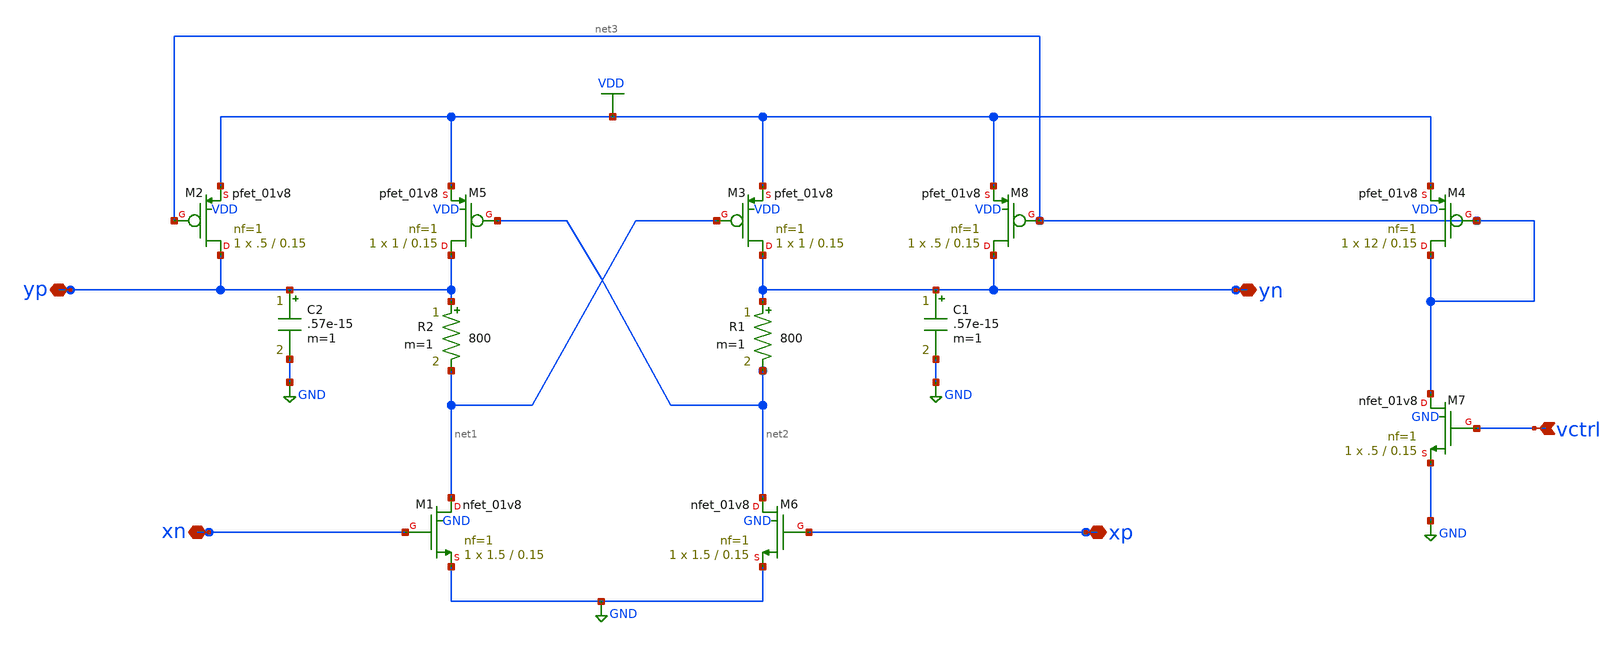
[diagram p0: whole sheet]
** sch_path: delay_cell/Delay_cell_2.sch
**.subckt Delay_cell_2 yp xn xp yn vctrl
*.iopin yp
*.iopin xn
*.iopin xp
*.iopin yn
*.ipin vctrl
R2 yp net1 800 m=1
R1 yn net2 800 m=1
XM4 net3 net3 VDD VDD sky130_fd_pr__pfet_01v8 L=0.15 W=12 nf=1 ad='int((nf+1)/2) * W/nf * 0.29' as='int((nf+2)/2) * W/nf * 0.29'
+ pd='2*int((nf+1)/2) * (W/nf + 0.29)' ps='2*int((nf+2)/2) * (W/nf + 0.29)' nrd='0.29 / W' nrs='0.29 / W'
+ sa=0 sb=0 sd=0 mult=1 m=1
XM7 net3 vctrl GND GND sky130_fd_pr__nfet_01v8 L=0.15 W=.5 nf=1 ad='int((nf+1)/2) * W/nf * 0.29' as='int((nf+2)/2) * W/nf * 0.29'
+ pd='2*int((nf+1)/2) * (W/nf + 0.29)' ps='2*int((nf+2)/2) * (W/nf + 0.29)' nrd='0.29 / W' nrs='0.29 / W'
+ sa=0 sb=0 sd=0 mult=1 m=1
C1 yn GND .57e-15 m=1
C2 yp GND .57e-15 m=1
XM1 net1 xn GND GND sky130_fd_pr__nfet_01v8 L=0.15 W=1.5 nf=1 ad='int((nf+1)/2) * W/nf * 0.29' as='int((nf+2)/2) * W/nf * 0.29'
+ pd='2*int((nf+1)/2) * (W/nf + 0.29)' ps='2*int((nf+2)/2) * (W/nf + 0.29)' nrd='0.29 / W' nrs='0.29 / W'
+ sa=0 sb=0 sd=0 mult=1 m=1
XM6 net2 xp GND GND sky130_fd_pr__nfet_01v8 L=0.15 W=1.5 nf=1 ad='int((nf+1)/2) * W/nf * 0.29' as='int((nf+2)/2) * W/nf * 0.29'
+ pd='2*int((nf+1)/2) * (W/nf + 0.29)' ps='2*int((nf+2)/2) * (W/nf + 0.29)' nrd='0.29 / W' nrs='0.29 / W'
+ sa=0 sb=0 sd=0 mult=1 m=1
XM2 yp net3 VDD VDD sky130_fd_pr__pfet_01v8 L=0.15 W=.5 nf=1 ad='int((nf+1)/2) * W/nf * 0.29' as='int((nf+2)/2) * W/nf * 0.29'
+ pd='2*int((nf+1)/2) * (W/nf + 0.29)' ps='2*int((nf+2)/2) * (W/nf + 0.29)' nrd='0.29 / W' nrs='0.29 / W'
+ sa=0 sb=0 sd=0 mult=1 m=1
XM3 yn net1 VDD VDD sky130_fd_pr__pfet_01v8 L=0.15 W=1 nf=1 ad='int((nf+1)/2) * W/nf * 0.29' as='int((nf+2)/2) * W/nf * 0.29'
+ pd='2*int((nf+1)/2) * (W/nf + 0.29)' ps='2*int((nf+2)/2) * (W/nf + 0.29)' nrd='0.29 / W' nrs='0.29 / W'
+ sa=0 sb=0 sd=0 mult=1 m=1
XM5 yp net2 VDD VDD sky130_fd_pr__pfet_01v8 L=0.15 W=1 nf=1 ad='int((nf+1)/2) * W/nf * 0.29' as='int((nf+2)/2) * W/nf * 0.29'
+ pd='2*int((nf+1)/2) * (W/nf + 0.29)' ps='2*int((nf+2)/2) * (W/nf + 0.29)' nrd='0.29 / W' nrs='0.29 / W'
+ sa=0 sb=0 sd=0 mult=1 m=1
XM8 yn net3 VDD VDD sky130_fd_pr__pfet_01v8 L=0.15 W=.5 nf=1 ad='int((nf+1)/2) * W/nf * 0.29' as='int((nf+2)/2) * W/nf * 0.29'
+ pd='2*int((nf+1)/2) * (W/nf + 0.29)' ps='2*int((nf+2)/2) * (W/nf + 0.29)' nrd='0.29 / W' nrs='0.29 / W'
+ sa=0 sb=0 sd=0 mult=1 m=1
**.ends
.GLOBAL GND
.GLOBAL VDD
.end
